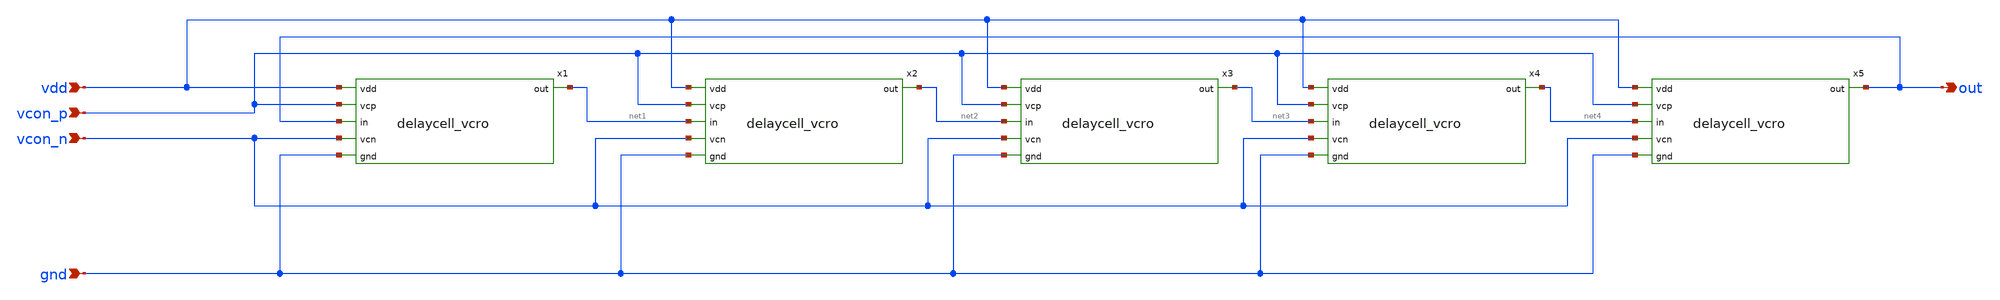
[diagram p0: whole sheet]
** sch_path: xschem/vcro_5elements.sch
**.subckt vcro_5elements vdd vcon_p vcon_n gnd out
*.ipin vdd
*.ipin vcon_p
*.ipin vcon_n
*.ipin gnd
*.opin out
x1 vdd vcon_p net1 out vcon_n gnd delaycell_vcro
x2 vdd vcon_p net2 net1 vcon_n gnd delaycell_vcro
x3 vdd vcon_p net3 net2 vcon_n gnd delaycell_vcro
x4 vdd vcon_p net4 net3 vcon_n gnd delaycell_vcro
x5 vdd vcon_p out net4 vcon_n gnd delaycell_vcro
**.ends
.end
